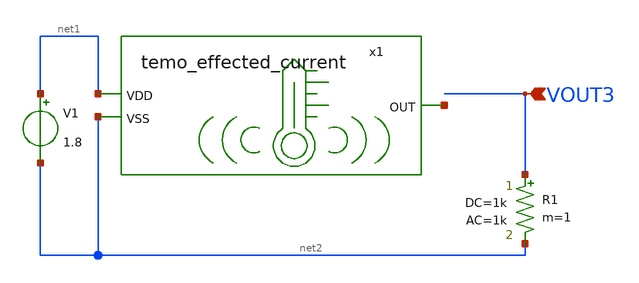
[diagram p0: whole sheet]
** sch_path: design/JNW_GR01_SKY130A/TB_OP6.sch
**.subckt TB_OP6 VOUT3
*.ipin VOUT3
R1 VOUT3 net2 1k ac=1k m=1
V1 net1 net2 1.8
x1 net1 net3 net2 temo_effected_current
**.ends
.end
